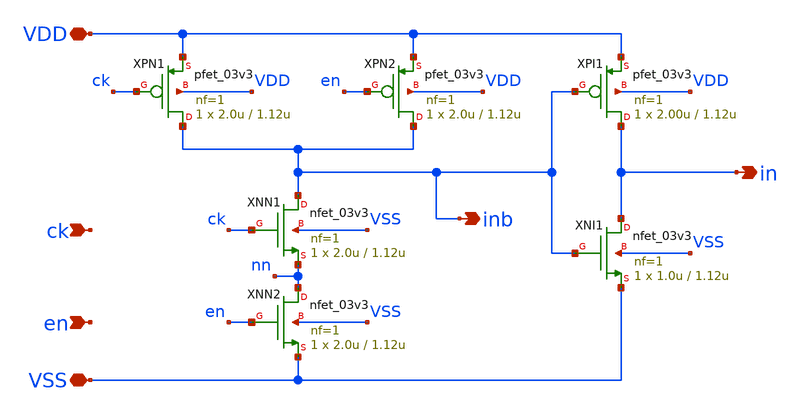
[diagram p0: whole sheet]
** sch_path: xschem/ck_FE.sch
**.subckt ck_FE VDD VSS ck en in inb
*.iopin VDD
*.iopin VSS
*.ipin ck
*.ipin en
*.opin in
*.opin inb
XPN1 inb ck VDD VDD pfet_03v3 L=1.12u W=2.0u nf=1 ad='int((nf+1)/2) * W/nf * 0.18u' as='int((nf+2)/2) * W/nf * 0.18u'
+ pd='2*int((nf+1)/2) * (W/nf + 0.18u)' ps='2*int((nf+2)/2) * (W/nf + 0.18u)' nrd='0.18u / W' nrs='0.18u / W'
+ sa=0 sb=0 sd=0 m=1 par=1
XPN2 inb en VDD VDD pfet_03v3 L=1.12u W=2.0u nf=1 ad='int((nf+1)/2) * W/nf * 0.18u' as='int((nf+2)/2) * W/nf * 0.18u'
+ pd='2*int((nf+1)/2) * (W/nf + 0.18u)' ps='2*int((nf+2)/2) * (W/nf + 0.18u)' nrd='0.18u / W' nrs='0.18u / W'
+ sa=0 sb=0 sd=0 m=1 par=1
XNN1 inb ck nn VSS nfet_03v3 L=1.12u W=2.0u nf=1 ad='int((nf+1)/2) * W/nf * 0.18u' as='int((nf+2)/2) * W/nf * 0.18u'
+ pd='2*int((nf+1)/2) * (W/nf + 0.18u)' ps='2*int((nf+2)/2) * (W/nf + 0.18u)' nrd='0.18u / W' nrs='0.18u / W'
+ sa=0 sb=0 sd=0 m=1 par=1
XNN2 nn en VSS VSS nfet_03v3 L=1.12u W=2.0u nf=1 ad='int((nf+1)/2) * W/nf * 0.18u' as='int((nf+2)/2) * W/nf * 0.18u'
+ pd='2*int((nf+1)/2) * (W/nf + 0.18u)' ps='2*int((nf+2)/2) * (W/nf + 0.18u)' nrd='0.18u / W' nrs='0.18u / W'
+ sa=0 sb=0 sd=0 m=1 par=1
XPI1 in inb VDD VDD pfet_03v3 L=1.12u W=2.00u nf=1 ad='int((nf+1)/2) * W/nf * 0.18u' as='int((nf+2)/2) * W/nf * 0.18u'
+ pd='2*int((nf+1)/2) * (W/nf + 0.18u)' ps='2*int((nf+2)/2) * (W/nf + 0.18u)' nrd='0.18u / W' nrs='0.18u / W'
+ sa=0 sb=0 sd=0 m=1 par=1
XNI1 in inb VSS VSS nfet_03v3 L=1.12u W=1.0u nf=1 ad='int((nf+1)/2) * W/nf * 0.18u' as='int((nf+2)/2) * W/nf * 0.18u'
+ pd='2*int((nf+1)/2) * (W/nf + 0.18u)' ps='2*int((nf+2)/2) * (W/nf + 0.18u)' nrd='0.18u / W' nrs='0.18u / W'
+ sa=0 sb=0 sd=0 m=1 par=1
**.ends
.end
